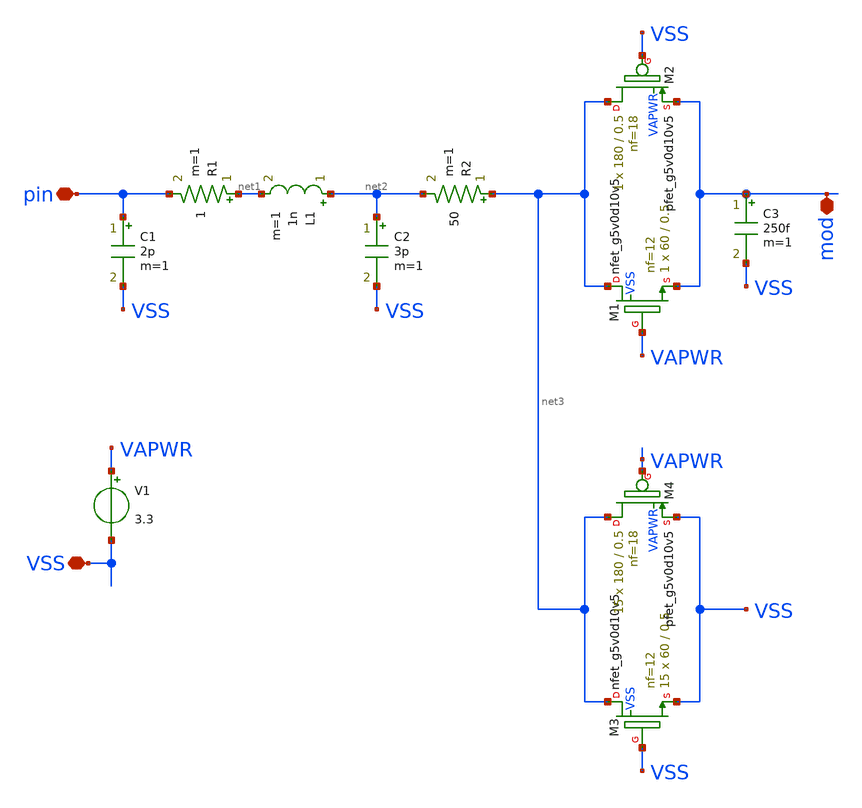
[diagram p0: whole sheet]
** sch_path: xschem/pad_model.sch
**.subckt pad_model pin mod VSS
*.iopin pin
*.iopin mod
*.iopin VSS
XM1 net3 VAPWR mod VSS sky130_fd_pr__nfet_g5v0d10v5 L=0.5 W=60 nf=12 ad='int((nf+1)/2) * W/nf * 0.29'
+ as='int((nf+2)/2) * W/nf * 0.29' pd='2*int((nf+1)/2) * (W/nf + 0.29)' ps='2*int((nf+2)/2) * (W/nf + 0.29)'
+ nrd='0.29 / W' nrs='0.29 / W' sa=0 sb=0 sd=0 mult=1 m=1
XM2 net3 VSS mod VAPWR sky130_fd_pr__pfet_g5v0d10v5 L=0.5 W=180 nf=18 ad='int((nf+1)/2) * W/nf * 0.29'
+ as='int((nf+2)/2) * W/nf * 0.29' pd='2*int((nf+1)/2) * (W/nf + 0.29)' ps='2*int((nf+2)/2) * (W/nf + 0.29)'
+ nrd='0.29 / W' nrs='0.29 / W' sa=0 sb=0 sd=0 mult=1 m=1
C1 pin VSS 2p m=1
V1 VAPWR VSS 3.3
R1 net1 pin 1 m=1
L1 net2 net1 1n m=1
C2 net2 VSS 3p m=1
R2 net3 net2 50 m=1
C3 mod VSS 250f m=1
XM3 net3 VSS VSS VSS sky130_fd_pr__nfet_g5v0d10v5 L=0.5 W=60 nf=12 ad='int((nf+1)/2) * W/nf * 0.29' as='int((nf+2)/2) * W/nf * 0.29'
+ pd='2*int((nf+1)/2) * (W/nf + 0.29)' ps='2*int((nf+2)/2) * (W/nf + 0.29)' nrd='0.29 / W' nrs='0.29 / W'
+ sa=0 sb=0 sd=0 mult=15 m=15
XM4 net3 VAPWR VSS VAPWR sky130_fd_pr__pfet_g5v0d10v5 L=0.5 W=180 nf=18 ad='int((nf+1)/2) * W/nf * 0.29'
+ as='int((nf+2)/2) * W/nf * 0.29' pd='2*int((nf+1)/2) * (W/nf + 0.29)' ps='2*int((nf+2)/2) * (W/nf + 0.29)'
+ nrd='0.29 / W' nrs='0.29 / W' sa=0 sb=0 sd=0 mult=15 m=15
**.ends
.end
